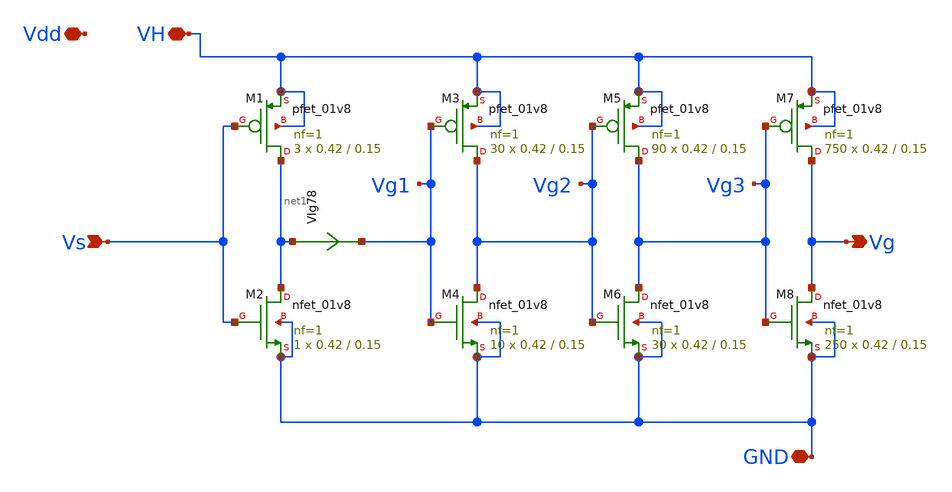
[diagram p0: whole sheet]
** sch_path: xschem/GD/GateDriver_woLS_fix.sch
**.subckt GateDriver_woLS_fix VH Vs Vg GND Vdd
*.iopin VH
*.ipin Vs
*.opin Vg
*.iopin GND
*.iopin Vdd
VIg78 net1 Vg1 0
.save i(vig78)
XM2 net1 Vs GND GND sky130_fd_pr__nfet_01v8 L=0.15 W=0.42 nf=1 ad='int((nf+1)/2) * W/nf * 0.29' as='int((nf+2)/2) * W/nf * 0.29'
+ pd='2*int((nf+1)/2) * (W/nf + 0.29)' ps='2*int((nf+2)/2) * (W/nf + 0.29)' nrd='0.29 / W' nrs='0.29 / W'
+ sa=0 sb=0 sd=0 mult=1 m=1
XM1 net1 Vs VH VH sky130_fd_pr__pfet_01v8 L=0.15 W=0.42 nf=1 ad='int((nf+1)/2) * W/nf * 0.29' as='int((nf+2)/2) * W/nf * 0.29'
+ pd='2*int((nf+1)/2) * (W/nf + 0.29)' ps='2*int((nf+2)/2) * (W/nf + 0.29)' nrd='0.29 / W' nrs='0.29 / W'
+ sa=0 sb=0 sd=0 mult=3 m=3
XM3 Vg2 Vg1 VH VH sky130_fd_pr__pfet_01v8 L=0.15 W=0.42 nf=1 ad='int((nf+1)/2) * W/nf * 0.29' as='int((nf+2)/2) * W/nf * 0.29'
+ pd='2*int((nf+1)/2) * (W/nf + 0.29)' ps='2*int((nf+2)/2) * (W/nf + 0.29)' nrd='0.29 / W' nrs='0.29 / W'
+ sa=0 sb=0 sd=0 mult=30 m=30
XM4 Vg2 Vg1 GND GND sky130_fd_pr__nfet_01v8 L=0.15 W=0.42 nf=1 ad='int((nf+1)/2) * W/nf * 0.29' as='int((nf+2)/2) * W/nf * 0.29'
+ pd='2*int((nf+1)/2) * (W/nf + 0.29)' ps='2*int((nf+2)/2) * (W/nf + 0.29)' nrd='0.29 / W' nrs='0.29 / W'
+ sa=0 sb=0 sd=0 mult=10 m=10
XM5 Vg3 Vg2 VH VH sky130_fd_pr__pfet_01v8 L=0.15 W=0.42 nf=1 ad='int((nf+1)/2) * W/nf * 0.29' as='int((nf+2)/2) * W/nf * 0.29'
+ pd='2*int((nf+1)/2) * (W/nf + 0.29)' ps='2*int((nf+2)/2) * (W/nf + 0.29)' nrd='0.29 / W' nrs='0.29 / W'
+ sa=0 sb=0 sd=0 mult=90 m=90
XM6 Vg3 Vg2 GND GND sky130_fd_pr__nfet_01v8 L=0.15 W=0.42 nf=1 ad='int((nf+1)/2) * W/nf * 0.29' as='int((nf+2)/2) * W/nf * 0.29'
+ pd='2*int((nf+1)/2) * (W/nf + 0.29)' ps='2*int((nf+2)/2) * (W/nf + 0.29)' nrd='0.29 / W' nrs='0.29 / W'
+ sa=0 sb=0 sd=0 mult=30 m=30
XM7 Vg Vg3 VH VH sky130_fd_pr__pfet_01v8 L=0.15 W=0.42 nf=1 ad='int((nf+1)/2) * W/nf * 0.29' as='int((nf+2)/2) * W/nf * 0.29'
+ pd='2*int((nf+1)/2) * (W/nf + 0.29)' ps='2*int((nf+2)/2) * (W/nf + 0.29)' nrd='0.29 / W' nrs='0.29 / W'
+ sa=0 sb=0 sd=0 mult=750 m=750
XM8 Vg Vg3 GND GND sky130_fd_pr__nfet_01v8 L=0.15 W=0.42 nf=1 ad='int((nf+1)/2) * W/nf * 0.29' as='int((nf+2)/2) * W/nf * 0.29'
+ pd='2*int((nf+1)/2) * (W/nf + 0.29)' ps='2*int((nf+2)/2) * (W/nf + 0.29)' nrd='0.29 / W' nrs='0.29 / W'
+ sa=0 sb=0 sd=0 mult=250 m=250
**.ends
.end
